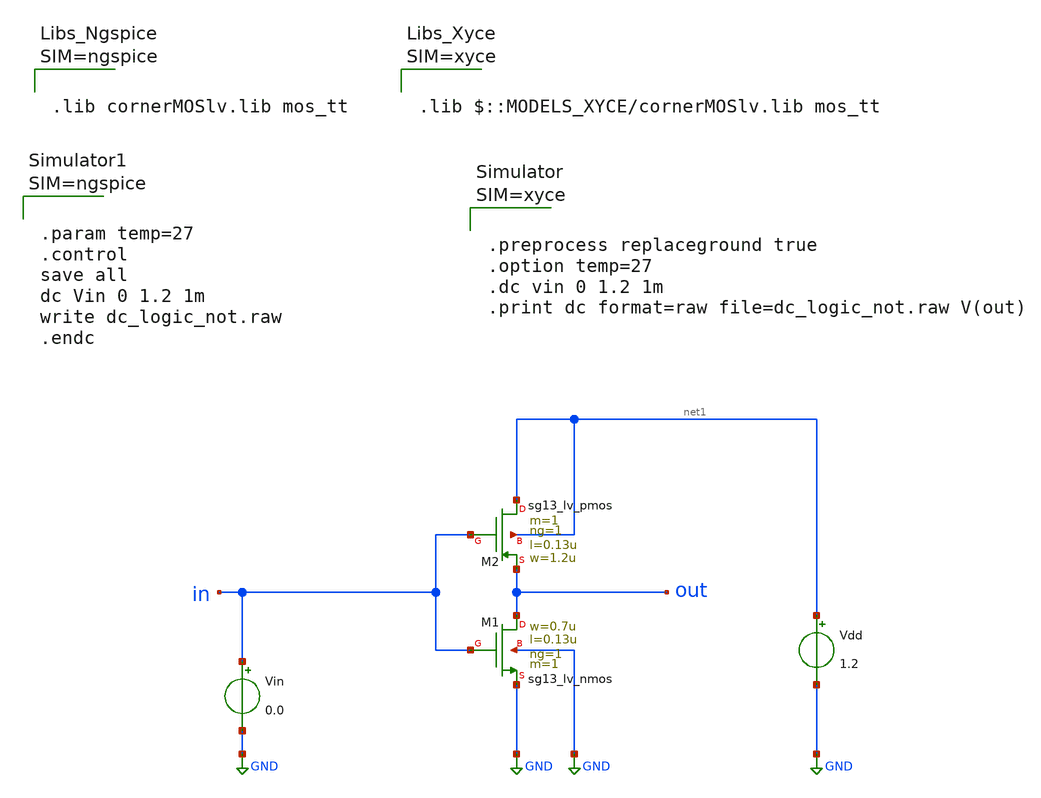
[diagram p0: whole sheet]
** sch_path: ihp-sg13g2/libs.tech/xschem/sg13g2_tests_xyce/dc_logic_not.sch
* Copyright 2023 IHP PDK Authors
**.subckt dc_logic_not
Vin in GND 0.0
Vdd net1 GND 1.2
XM1 out in GND GND sg13_lv_nmos w=0.7u l=0.13u ng=1 m=1 mm_ok=1
XM2 net1 in out net1 sg13_lv_pmos w=1.2u l=0.13u ng=1 m=1 mm_ok=1
**** begin user architecture code









.lib cornerMOSlv.lib mos_tt






.param temp=27
.control
save all
dc Vin 0 1.2 1m
write dc_logic_not.raw
.endc



**** end user architecture code
**.ends
.GLOBAL GND
.end
